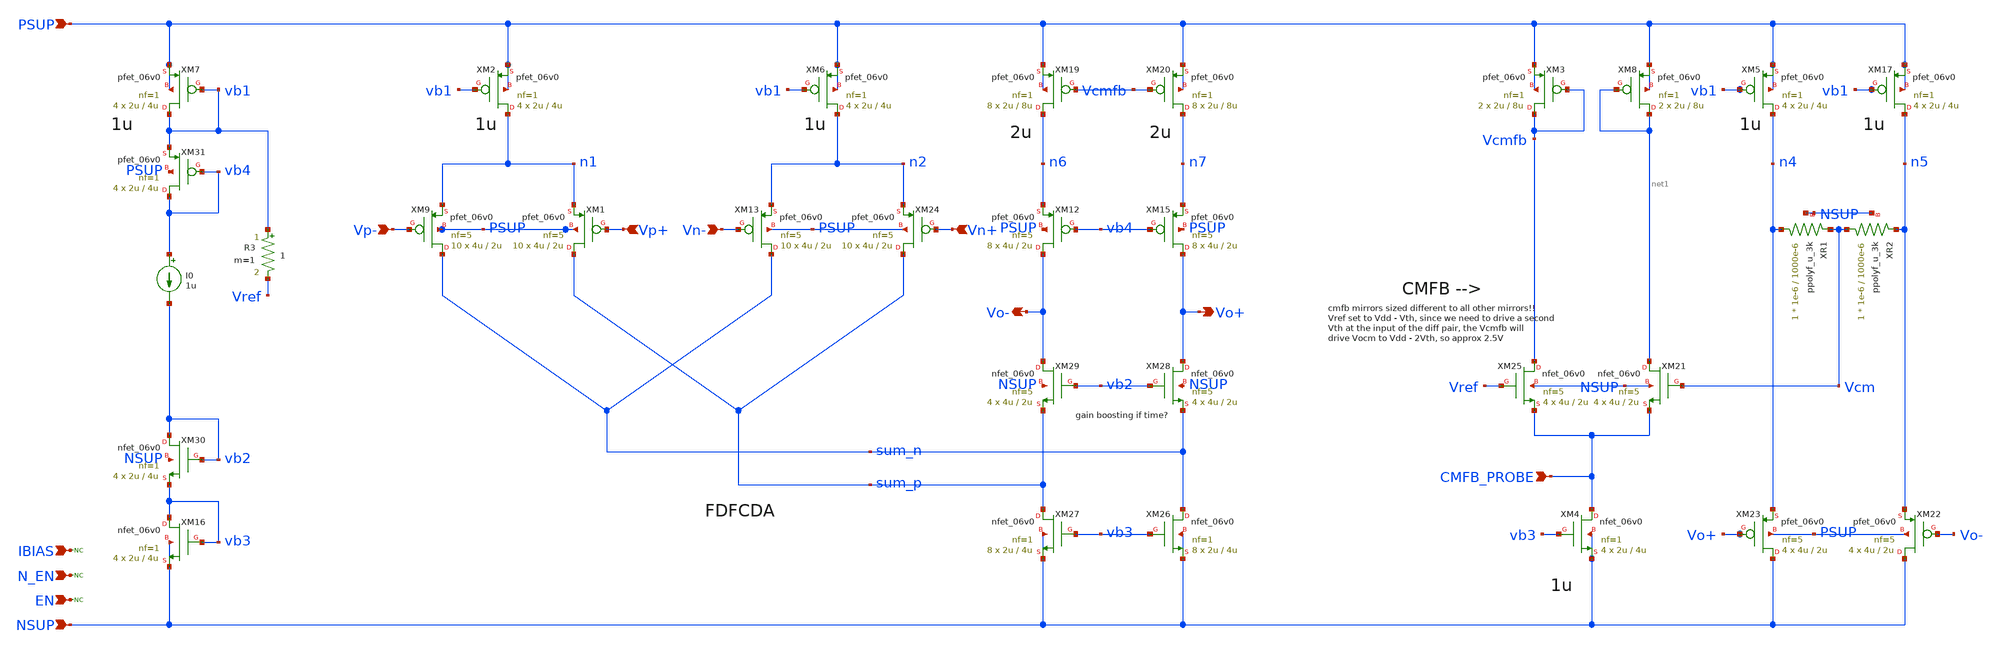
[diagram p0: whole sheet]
** sch_path: xschem/blocks/fdda/fdda.sch
**.subckt fdda PSUP NSUP N_EN EN IBIAS Vp+ Vp- Vn+ Vn- Vo+ Vo- CMFB_PROBE
*.ipin PSUP
*.ipin NSUP
*.ipin N_EN
*.ipin EN
*.ipin IBIAS
*.ipin Vp+
*.ipin Vp-
*.ipin Vn+
*.ipin Vn-
*.opin Vo+
*.opin Vo-
*.ipin CMFB_PROBE
* noconn N_EN
* noconn EN
I0 vb4 vb2 1u
XM7 vb1 vb1 PSUP PSUP pfet_06v0 L=4u W=2u nf=1 ad='int((nf+1)/2) * W/nf * 0.18u' as='int((nf+2)/2) * W/nf * 0.18u'
+ pd='2*int((nf+1)/2) * (W/nf + 0.18u)' ps='2*int((nf+2)/2) * (W/nf + 0.18u)' nrd='0.18u / W' nrs='0.18u / W'
+ sa=0 sb=0 sd=0 m=4
* noconn IBIAS
XM16 vb3 vb3 NSUP NSUP nfet_06v0 L=4u W=2u nf=1 ad='int((nf+1)/2) * W/nf * 0.18u' as='int((nf+2)/2) * W/nf * 0.18u'
+ pd='2*int((nf+1)/2) * (W/nf + 0.18u)' ps='2*int((nf+2)/2) * (W/nf + 0.18u)' nrd='0.18u / W' nrs='0.18u / W'
+ sa=0 sb=0 sd=0 m=4
XM9 sum_n Vp- n1 PSUP pfet_06v0 L=2u W=4u nf=5 ad='int((nf+1)/2) * W/nf * 0.18u' as='int((nf+2)/2) * W/nf * 0.18u'
+ pd='2*int((nf+1)/2) * (W/nf + 0.18u)' ps='2*int((nf+2)/2) * (W/nf + 0.18u)' nrd='0.18u / W' nrs='0.18u / W'
+ sa=0 sb=0 sd=0 m=10
XM1 sum_p Vp+ n1 PSUP pfet_06v0 L=2u W=4u nf=5 ad='int((nf+1)/2) * W/nf * 0.18u' as='int((nf+2)/2) * W/nf * 0.18u'
+ pd='2*int((nf+1)/2) * (W/nf + 0.18u)' ps='2*int((nf+2)/2) * (W/nf + 0.18u)' nrd='0.18u / W' nrs='0.18u / W'
+ sa=0 sb=0 sd=0 m=10
XM2 n1 vb1 PSUP PSUP pfet_06v0 L=4u W=2u nf=1 ad='int((nf+1)/2) * W/nf * 0.18u' as='int((nf+2)/2) * W/nf * 0.18u'
+ pd='2*int((nf+1)/2) * (W/nf + 0.18u)' ps='2*int((nf+2)/2) * (W/nf + 0.18u)' nrd='0.18u / W' nrs='0.18u / W'
+ sa=0 sb=0 sd=0 m=4
XM6 n2 vb1 PSUP PSUP pfet_06v0 L=4u W=2u nf=1 ad='int((nf+1)/2) * W/nf * 0.18u' as='int((nf+2)/2) * W/nf * 0.18u'
+ pd='2*int((nf+1)/2) * (W/nf + 0.18u)' ps='2*int((nf+2)/2) * (W/nf + 0.18u)' nrd='0.18u / W' nrs='0.18u / W'
+ sa=0 sb=0 sd=0 m=4
XM24 sum_p Vn+ n2 PSUP pfet_06v0 L=2u W=4u nf=5 ad='int((nf+1)/2) * W/nf * 0.18u' as='int((nf+2)/2) * W/nf * 0.18u'
+ pd='2*int((nf+1)/2) * (W/nf + 0.18u)' ps='2*int((nf+2)/2) * (W/nf + 0.18u)' nrd='0.18u / W' nrs='0.18u / W'
+ sa=0 sb=0 sd=0 m=10
XM13 sum_n Vn- n2 PSUP pfet_06v0 L=2u W=4u nf=5 ad='int((nf+1)/2) * W/nf * 0.18u' as='int((nf+2)/2) * W/nf * 0.18u'
+ pd='2*int((nf+1)/2) * (W/nf + 0.18u)' ps='2*int((nf+2)/2) * (W/nf + 0.18u)' nrd='0.18u / W' nrs='0.18u / W'
+ sa=0 sb=0 sd=0 m=10
XM12 Vo- vb4 n6 PSUP pfet_06v0 L=2u W=4u nf=5 ad='int((nf+1)/2) * W/nf * 0.18u' as='int((nf+2)/2) * W/nf * 0.18u'
+ pd='2*int((nf+1)/2) * (W/nf + 0.18u)' ps='2*int((nf+2)/2) * (W/nf + 0.18u)' nrd='0.18u / W' nrs='0.18u / W'
+ sa=0 sb=0 sd=0 m=8
XM15 Vo+ vb4 n7 PSUP pfet_06v0 L=2u W=4u nf=5 ad='int((nf+1)/2) * W/nf * 0.18u' as='int((nf+2)/2) * W/nf * 0.18u'
+ pd='2*int((nf+1)/2) * (W/nf + 0.18u)' ps='2*int((nf+2)/2) * (W/nf + 0.18u)' nrd='0.18u / W' nrs='0.18u / W'
+ sa=0 sb=0 sd=0 m=8
XM19 n6 Vcmfb PSUP PSUP pfet_06v0 L=8u W=2u nf=1 ad='int((nf+1)/2) * W/nf * 0.18u' as='int((nf+2)/2) * W/nf * 0.18u'
+ pd='2*int((nf+1)/2) * (W/nf + 0.18u)' ps='2*int((nf+2)/2) * (W/nf + 0.18u)' nrd='0.18u / W' nrs='0.18u / W'
+ sa=0 sb=0 sd=0 m=8
XM20 n7 Vcmfb PSUP PSUP pfet_06v0 L=8u W=2u nf=1 ad='int((nf+1)/2) * W/nf * 0.18u' as='int((nf+2)/2) * W/nf * 0.18u'
+ pd='2*int((nf+1)/2) * (W/nf + 0.18u)' ps='2*int((nf+2)/2) * (W/nf + 0.18u)' nrd='0.18u / W' nrs='0.18u / W'
+ sa=0 sb=0 sd=0 m=8
XM26 sum_n vb3 NSUP NSUP nfet_06v0 L=4u W=2u nf=1 ad='int((nf+1)/2) * W/nf * 0.18u' as='int((nf+2)/2) * W/nf * 0.18u'
+ pd='2*int((nf+1)/2) * (W/nf + 0.18u)' ps='2*int((nf+2)/2) * (W/nf + 0.18u)' nrd='0.18u / W' nrs='0.18u / W'
+ sa=0 sb=0 sd=0 m=8
XM27 sum_p vb3 NSUP NSUP nfet_06v0 L=4u W=2u nf=1 ad='int((nf+1)/2) * W/nf * 0.18u' as='int((nf+2)/2) * W/nf * 0.18u'
+ pd='2*int((nf+1)/2) * (W/nf + 0.18u)' ps='2*int((nf+2)/2) * (W/nf + 0.18u)' nrd='0.18u / W' nrs='0.18u / W'
+ sa=0 sb=0 sd=0 m=8
XM28 Vo+ vb2 sum_n NSUP nfet_06v0 L=2u W=4u nf=5 ad='int((nf+1)/2) * W/nf * 0.18u' as='int((nf+2)/2) * W/nf * 0.18u'
+ pd='2*int((nf+1)/2) * (W/nf + 0.18u)' ps='2*int((nf+2)/2) * (W/nf + 0.18u)' nrd='0.18u / W' nrs='0.18u / W'
+ sa=0 sb=0 sd=0 m=4
XM29 Vo- vb2 sum_p NSUP nfet_06v0 L=2u W=4u nf=5 ad='int((nf+1)/2) * W/nf * 0.18u' as='int((nf+2)/2) * W/nf * 0.18u'
+ pd='2*int((nf+1)/2) * (W/nf + 0.18u)' ps='2*int((nf+2)/2) * (W/nf + 0.18u)' nrd='0.18u / W' nrs='0.18u / W'
+ sa=0 sb=0 sd=0 m=4
XM30 vb2 vb2 vb3 NSUP nfet_06v0 L=4u W=2u nf=1 ad='int((nf+1)/2) * W/nf * 0.18u' as='int((nf+2)/2) * W/nf * 0.18u'
+ pd='2*int((nf+1)/2) * (W/nf + 0.18u)' ps='2*int((nf+2)/2) * (W/nf + 0.18u)' nrd='0.18u / W' nrs='0.18u / W'
+ sa=0 sb=0 sd=0 m=4
XM31 vb4 vb4 vb1 PSUP pfet_06v0 L=4u W=2u nf=1 ad='int((nf+1)/2) * W/nf * 0.18u' as='int((nf+2)/2) * W/nf * 0.18u'
+ pd='2*int((nf+1)/2) * (W/nf + 0.18u)' ps='2*int((nf+2)/2) * (W/nf + 0.18u)' nrd='0.18u / W' nrs='0.18u / W'
+ sa=0 sb=0 sd=0 m=4
XM3 Vcmfb Vcmfb PSUP PSUP pfet_06v0 L=8u W=2u nf=1 ad='int((nf+1)/2) * W/nf * 0.18u' as='int((nf+2)/2) * W/nf * 0.18u'
+ pd='2*int((nf+1)/2) * (W/nf + 0.18u)' ps='2*int((nf+2)/2) * (W/nf + 0.18u)' nrd='0.18u / W' nrs='0.18u / W'
+ sa=0 sb=0 sd=0 m=2
XM8 net1 net1 PSUP PSUP pfet_06v0 L=8u W=2u nf=1 ad='int((nf+1)/2) * W/nf * 0.18u' as='int((nf+2)/2) * W/nf * 0.18u'
+ pd='2*int((nf+1)/2) * (W/nf + 0.18u)' ps='2*int((nf+2)/2) * (W/nf + 0.18u)' nrd='0.18u / W' nrs='0.18u / W'
+ sa=0 sb=0 sd=0 m=2
XM21 net1 Vcm CMFB_PROBE NSUP nfet_06v0 L=2u W=4u nf=5 ad='int((nf+1)/2) * W/nf * 0.18u' as='int((nf+2)/2) * W/nf * 0.18u'
+ pd='2*int((nf+1)/2) * (W/nf + 0.18u)' ps='2*int((nf+2)/2) * (W/nf + 0.18u)' nrd='0.18u / W' nrs='0.18u / W'
+ sa=0 sb=0 sd=0 m=4
XM25 Vcmfb Vref CMFB_PROBE NSUP nfet_06v0 L=2u W=4u nf=5 ad='int((nf+1)/2) * W/nf * 0.18u' as='int((nf+2)/2) * W/nf * 0.18u'
+ pd='2*int((nf+1)/2) * (W/nf + 0.18u)' ps='2*int((nf+2)/2) * (W/nf + 0.18u)' nrd='0.18u / W' nrs='0.18u / W'
+ sa=0 sb=0 sd=0 m=4
XM4 CMFB_PROBE vb3 NSUP NSUP nfet_06v0 L=4u W=2u nf=1 ad='int((nf+1)/2) * W/nf * 0.18u' as='int((nf+2)/2) * W/nf * 0.18u'
+ pd='2*int((nf+1)/2) * (W/nf + 0.18u)' ps='2*int((nf+2)/2) * (W/nf + 0.18u)' nrd='0.18u / W' nrs='0.18u / W'
+ sa=0 sb=0 sd=0 m=4
XM22 NSUP Vo- n5 PSUP pfet_06v0 L=2u W=4u nf=5 ad='int((nf+1)/2) * W/nf * 0.18u' as='int((nf+2)/2) * W/nf * 0.18u'
+ pd='2*int((nf+1)/2) * (W/nf + 0.18u)' ps='2*int((nf+2)/2) * (W/nf + 0.18u)' nrd='0.18u / W' nrs='0.18u / W'
+ sa=0 sb=0 sd=0 m=4
XM23 NSUP Vo+ n4 PSUP pfet_06v0 L=2u W=4u nf=5 ad='int((nf+1)/2) * W/nf * 0.18u' as='int((nf+2)/2) * W/nf * 0.18u'
+ pd='2*int((nf+1)/2) * (W/nf + 0.18u)' ps='2*int((nf+2)/2) * (W/nf + 0.18u)' nrd='0.18u / W' nrs='0.18u / W'
+ sa=0 sb=0 sd=0 m=4
XR1 n4 Vcm NSUP ppolyf_u_3k r_width=1e-6 r_length=1000e-6 m=1
XR2 Vcm n5 NSUP ppolyf_u_3k r_width=1e-6 r_length=1000e-6 m=1
XM5 n4 vb1 PSUP PSUP pfet_06v0 L=4u W=2u nf=1 ad='int((nf+1)/2) * W/nf * 0.18u' as='int((nf+2)/2) * W/nf * 0.18u'
+ pd='2*int((nf+1)/2) * (W/nf + 0.18u)' ps='2*int((nf+2)/2) * (W/nf + 0.18u)' nrd='0.18u / W' nrs='0.18u / W'
+ sa=0 sb=0 sd=0 m=4
XM17 n5 vb1 PSUP PSUP pfet_06v0 L=4u W=2u nf=1 ad='int((nf+1)/2) * W/nf * 0.18u' as='int((nf+2)/2) * W/nf * 0.18u'
+ pd='2*int((nf+1)/2) * (W/nf + 0.18u)' ps='2*int((nf+2)/2) * (W/nf + 0.18u)' nrd='0.18u / W' nrs='0.18u / W'
+ sa=0 sb=0 sd=0 m=4
R3 vb1 Vref 1 m=1
**.ends
.end
